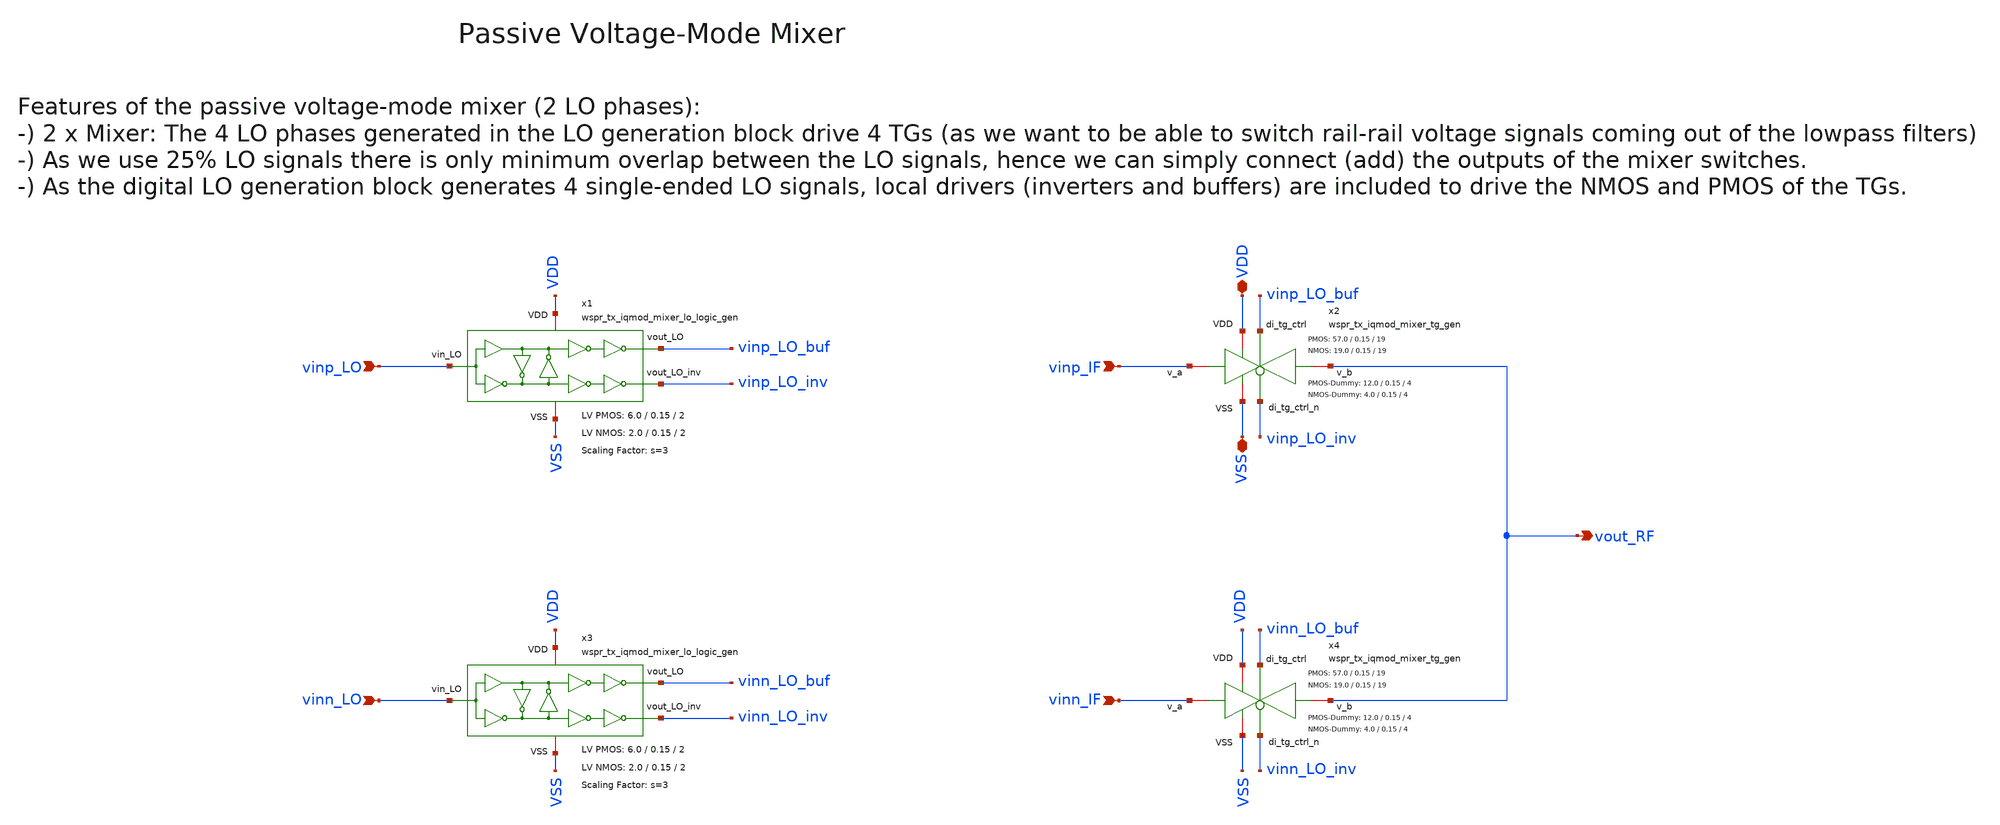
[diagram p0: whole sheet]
** sch_path: sky130/xschem/generic/wspr_tx_iqmod_mixer_gen.sch
**.subckt wspr_tx_iqmod_mixer_gen VDD VSS vinp_IF vinn_IF vout_RF vinp_LO vinn_LO
*.iopin VDD
*.iopin VSS
*.ipin vinp_IF
*.ipin vinn_IF
*.opin vout_RF
*.ipin vinp_LO
*.ipin vinn_LO
x1 VDD vinp_LO vinp_LO_buf VSS vinp_LO_inv wspr_tx_iqmod_mixer_lo_logic_gen W_P=6.0 L_P=0.15 NF_P=2
+ W_N=2.0 L_N=0.15 NF_N=2 s=3
x3 VDD vinn_LO vinn_LO_buf VSS vinn_LO_inv wspr_tx_iqmod_mixer_lo_logic_gen W_P=6.0 L_P=0.15 NF_P=2
+ W_N=2.0 L_N=0.15 NF_N=2 s=3
x2 VDD vinp_LO_buf VSS vout_RF vinp_IF vinp_LO_inv wspr_tx_iqmod_mixer_tg_gen W_P=57.0 L_P=0.15
+ NF_P=19 W_N=19.0 L_N=0.15 NF_N=19 W_P_D=12.0 L_P_D=0.15 NF_P_D=4 W_N_D=4.0 L_N_D=0.15 NF_N_D=4
x4 VDD vinn_LO_buf VSS vout_RF vinn_IF vinn_LO_inv wspr_tx_iqmod_mixer_tg_gen W_P=57.0 L_P=0.15
+ NF_P=19 W_N=19.0 L_N=0.15 NF_N=19 W_P_D=12.0 L_P_D=0.15 NF_P_D=4 W_N_D=4.0 L_N_D=0.15 NF_N_D=4
**.ends
.end
